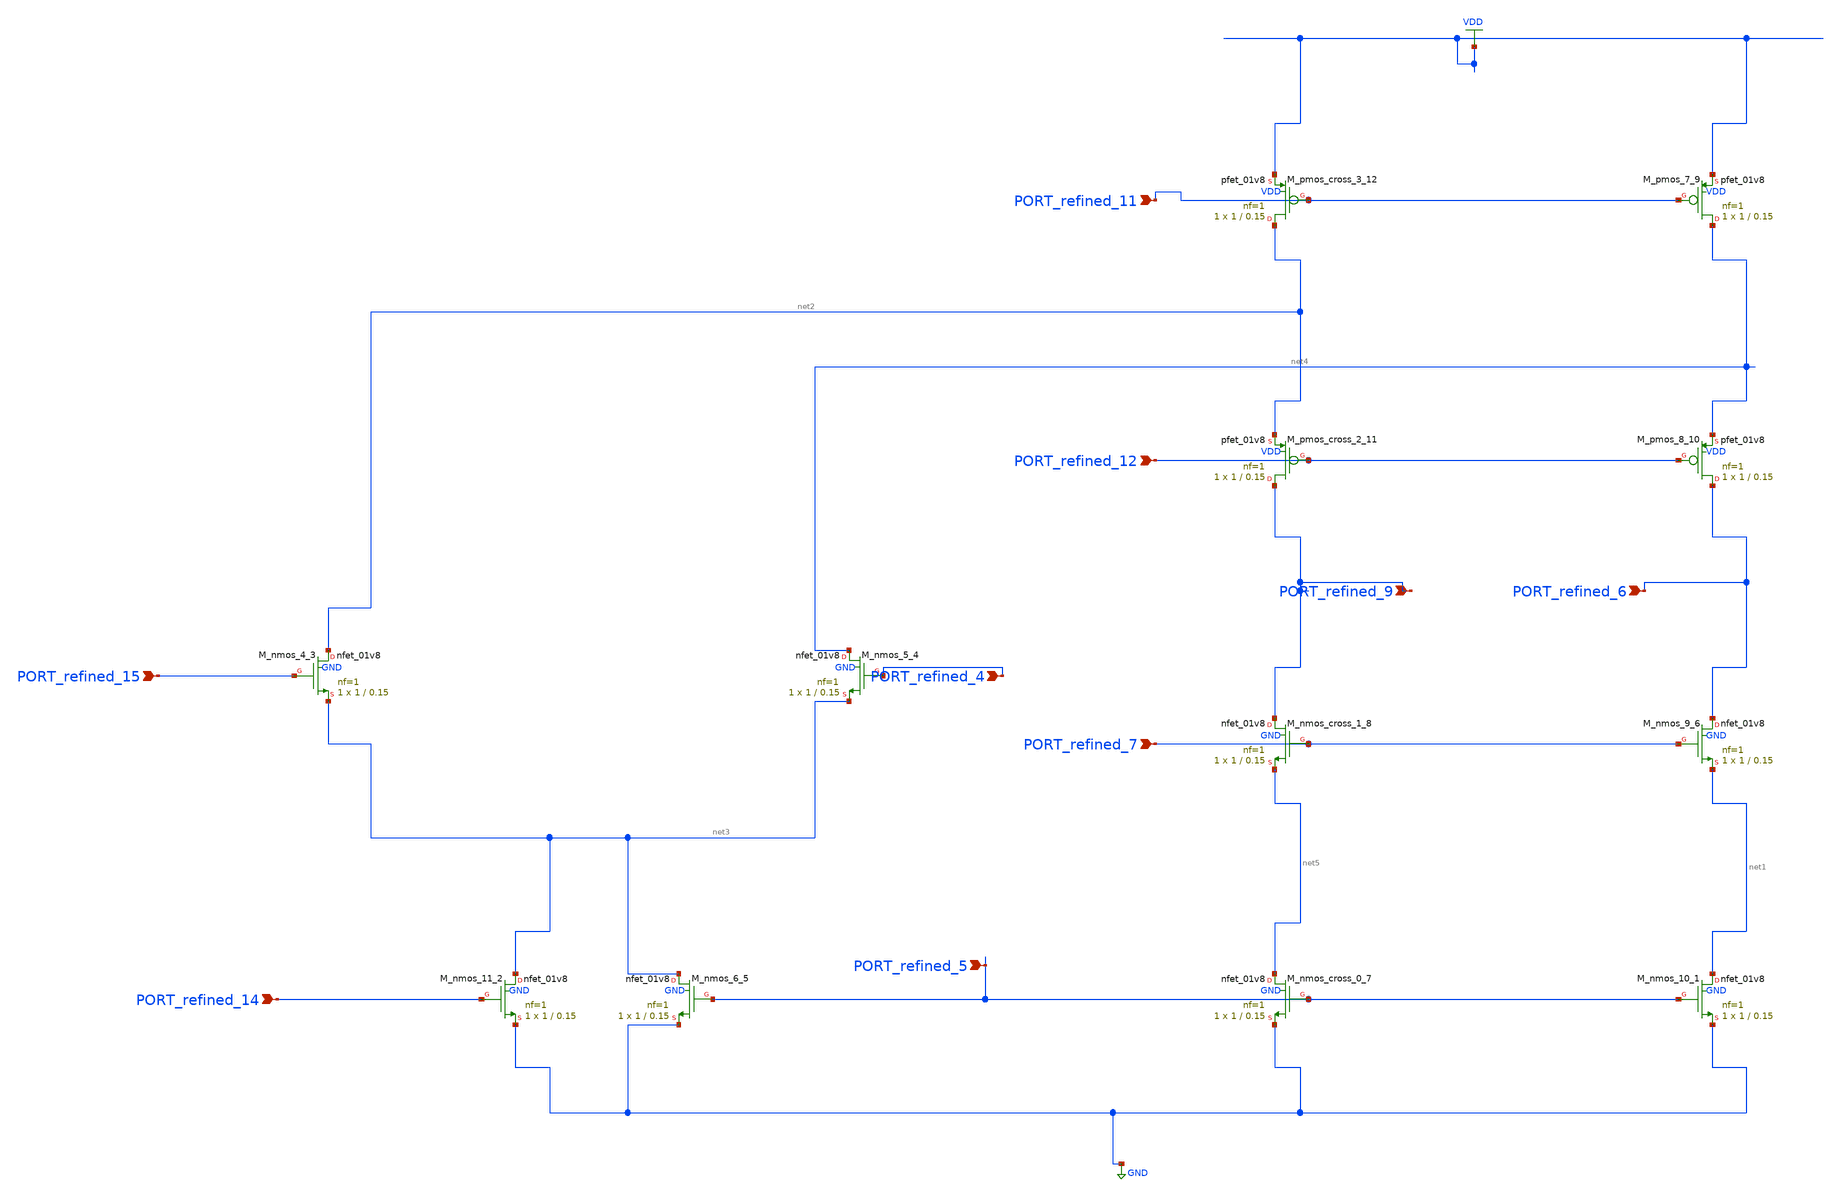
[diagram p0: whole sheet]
** sch_path: schematics/Image2Net/125.sch
**.subckt 125 PORT_refined_12 PORT_refined_7 PORT_refined_9 PORT_refined_6 PORT_refined_11
*+ PORT_refined_4 PORT_refined_5 PORT_refined_14 PORT_refined_15
*.ipin PORT_refined_12
*.ipin PORT_refined_7
*.ipin PORT_refined_9
*.ipin PORT_refined_6
*.ipin PORT_refined_11
*.ipin PORT_refined_4
*.ipin PORT_refined_5
*.ipin PORT_refined_14
*.ipin PORT_refined_15
XM_nmos_10_1 net1 PORT_refined_5 GND GND sky130_fd_pr__nfet_01v8 L=0.15 W=1 nf=1 ad='int((1 + 1)/2) * 1 / 1 * 0.29'
+ as='int((1 + 2)/2) * 1 / 1 * 0.29' pd='2*int((1 + 1)/2) * (1 / 1 + 0.29)' ps='2*int((1 + 2)/2) * (1 / 1 + 0.29)'
+ nrd='0.29 / 1 ' nrs='0.29 / 1 ' sa=0 sb=0 sd=0 mult=1 m=1
XM_nmos_11_2 net3 PORT_refined_14 GND GND sky130_fd_pr__nfet_01v8 L=0.15 W=1 nf=1 ad='int((1 + 1)/2) * 1 / 1 * 0.29'
+ as='int((1 + 2)/2) * 1 / 1 * 0.29' pd='2*int((1 + 1)/2) * (1 / 1 + 0.29)' ps='2*int((1 + 2)/2) * (1 / 1 + 0.29)'
+ nrd='0.29 / 1 ' nrs='0.29 / 1 ' sa=0 sb=0 sd=0 mult=1 m=1
XM_nmos_4_3 net2 PORT_refined_15 net3 GND sky130_fd_pr__nfet_01v8 L=0.15 W=1 nf=1 ad='int((1 + 1)/2) * 1 / 1 * 0.29'
+ as='int((1 + 2)/2) * 1 / 1 * 0.29' pd='2*int((1 + 1)/2) * (1 / 1 + 0.29)' ps='2*int((1 + 2)/2) * (1 / 1 + 0.29)'
+ nrd='0.29 / 1 ' nrs='0.29 / 1 ' sa=0 sb=0 sd=0 mult=1 m=1
XM_nmos_5_4 net4 PORT_refined_4 net3 GND sky130_fd_pr__nfet_01v8 L=0.15 W=1 nf=1 ad='int((1 + 1)/2) * 1 / 1 * 0.29'
+ as='int((1 + 2)/2) * 1 / 1 * 0.29' pd='2*int((1 + 1)/2) * (1 / 1 + 0.29)' ps='2*int((1 + 2)/2) * (1 / 1 + 0.29)'
+ nrd='0.29 / 1 ' nrs='0.29 / 1 ' sa=0 sb=0 sd=0 mult=1 m=1
XM_nmos_6_5 net3 PORT_refined_5 GND GND sky130_fd_pr__nfet_01v8 L=0.15 W=1 nf=1 ad='int((1 + 1)/2) * 1 / 1 * 0.29'
+ as='int((1 + 2)/2) * 1 / 1 * 0.29' pd='2*int((1 + 1)/2) * (1 / 1 + 0.29)' ps='2*int((1 + 2)/2) * (1 / 1 + 0.29)'
+ nrd='0.29 / 1 ' nrs='0.29 / 1 ' sa=0 sb=0 sd=0 mult=1 m=1
XM_nmos_9_6 PORT_refined_6 PORT_refined_7 net1 GND sky130_fd_pr__nfet_01v8 L=0.15 W=1 nf=1 ad='int((1 + 1)/2) * 1 / 1 * 0.29'
+ as='int((1 + 2)/2) * 1 / 1 * 0.29' pd='2*int((1 + 1)/2) * (1 / 1 + 0.29)' ps='2*int((1 + 2)/2) * (1 / 1 + 0.29)'
+ nrd='0.29 / 1 ' nrs='0.29 / 1 ' sa=0 sb=0 sd=0 mult=1 m=1
XM_nmos_cross_0_7 net5 PORT_refined_5 GND GND sky130_fd_pr__nfet_01v8 L=0.15 W=1 nf=1 ad='int((1 + 1)/2) * 1 / 1 * 0.29'
+ as='int((1 + 2)/2) * 1 / 1 * 0.29' pd='2*int((1 + 1)/2) * (1 / 1 + 0.29)' ps='2*int((1 + 2)/2) * (1 / 1 + 0.29)'
+ nrd='0.29 / 1 ' nrs='0.29 / 1 ' sa=0 sb=0 sd=0 mult=1 m=1
XM_nmos_cross_1_8 PORT_refined_9 PORT_refined_7 net5 GND sky130_fd_pr__nfet_01v8 L=0.15 W=1 nf=1 ad='int((1 + 1)/2) * 1 / 1 * 0.29'
+ as='int((1 + 2)/2) * 1 / 1 * 0.29' pd='2*int((1 + 1)/2) * (1 / 1 + 0.29)' ps='2*int((1 + 2)/2) * (1 / 1 + 0.29)'
+ nrd='0.29 / 1 ' nrs='0.29 / 1 ' sa=0 sb=0 sd=0 mult=1 m=1
XM_pmos_7_9 net4 PORT_refined_11 VDD VDD sky130_fd_pr__pfet_01v8 L=0.15 W=1 nf=1 ad='int((1 + 1)/2) * 1 / 1 * 0.29'
+ as='int((1 + 2)/2) * 1 / 1 * 0.29' pd='2*int((1 + 1)/2) * (1 / 1 + 0.29)' ps='2*int((1 + 2)/2) * (1 / 1 + 0.29)'
+ nrd='0.29 / 1 ' nrs='0.29 / 1 ' sa=0 sb=0 sd=0 mult=1 m=1
XM_pmos_8_10 PORT_refined_6 PORT_refined_12 net4 VDD sky130_fd_pr__pfet_01v8 L=0.15 W=1 nf=1 ad='int((1 + 1)/2) * 1 / 1 * 0.29'
+ as='int((1 + 2)/2) * 1 / 1 * 0.29' pd='2*int((1 + 1)/2) * (1 / 1 + 0.29)' ps='2*int((1 + 2)/2) * (1 / 1 + 0.29)'
+ nrd='0.29 / 1 ' nrs='0.29 / 1 ' sa=0 sb=0 sd=0 mult=1 m=1
XM_pmos_cross_2_11 PORT_refined_9 PORT_refined_12 net2 VDD sky130_fd_pr__pfet_01v8 L=0.15 W=1 nf=1 ad='int((1 + 1)/2) * 1 / 1 * 0.29'
+ as='int((1 + 2)/2) * 1 / 1 * 0.29' pd='2*int((1 + 1)/2) * (1 / 1 + 0.29)' ps='2*int((1 + 2)/2) * (1 / 1 + 0.29)'
+ nrd='0.29 / 1 ' nrs='0.29 / 1 ' sa=0 sb=0 sd=0 mult=1 m=1
XM_pmos_cross_3_12 net2 PORT_refined_11 VDD VDD sky130_fd_pr__pfet_01v8 L=0.15 W=1 nf=1 ad='int((1 + 1)/2) * 1 / 1 * 0.29'
+ as='int((1 + 2)/2) * 1 / 1 * 0.29' pd='2*int((1 + 1)/2) * (1 / 1 + 0.29)' ps='2*int((1 + 2)/2) * (1 / 1 + 0.29)'
+ nrd='0.29 / 1 ' nrs='0.29 / 1 ' sa=0 sb=0 sd=0 mult=1 m=1
**.ends
.GLOBAL GND
.GLOBAL VDD
.end
